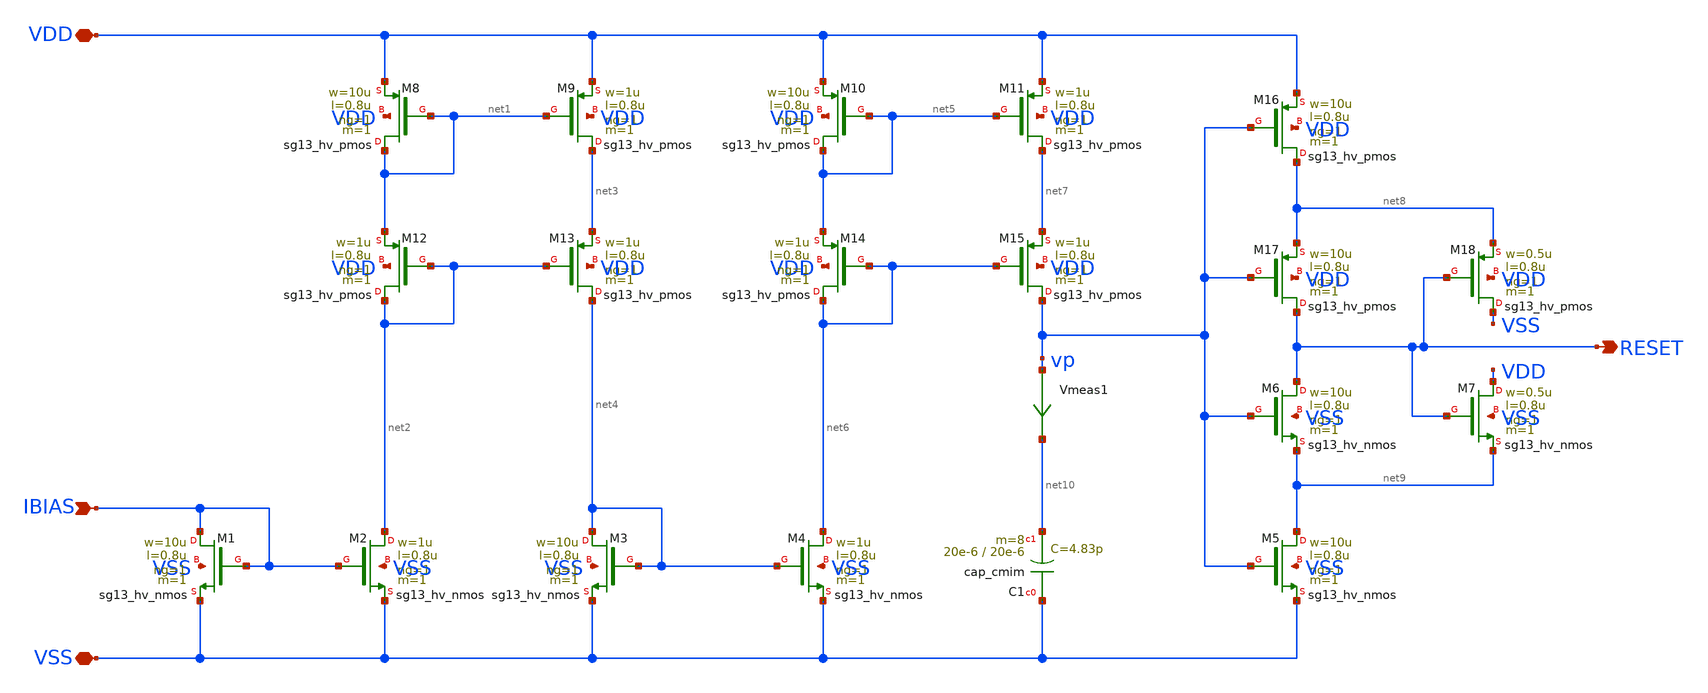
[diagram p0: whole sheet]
** sch_path: ip/por/xschem/por.sch
**.subckt por VSS VDD RESET IBIAS
*.iopin VSS
*.iopin VDD
*.opin RESET
*.ipin IBIAS
XM8 net1 net1 VDD VDD sg13_hv_pmos w=10u l=0.8u ng=1 m=1 mm_ok=1
Vmeas1 vp net10 0
.save i(vmeas1)
XM12 net2 net2 net1 VDD sg13_hv_pmos w=1u l=0.8u ng=1 m=1 mm_ok=1
XM1 IBIAS IBIAS VSS VSS sg13_hv_nmos w=10u l=0.8u ng=1 m=1 mm_ok=1
XM2 net2 IBIAS VSS VSS sg13_hv_nmos w=1u l=0.8u ng=1 m=1 mm_ok=1
XM9 net3 net1 VDD VDD sg13_hv_pmos w=1u l=0.8u ng=1 m=1 mm_ok=1
XM13 net4 net2 net3 VDD sg13_hv_pmos w=1u l=0.8u ng=1 m=1 mm_ok=1
XM3 net4 net4 VSS VSS sg13_hv_nmos w=10u l=0.8u ng=1 m=1 mm_ok=1
XM10 net5 net5 VDD VDD sg13_hv_pmos w=10u l=0.8u ng=1 m=1 mm_ok=1
XM14 net6 net6 net5 VDD sg13_hv_pmos w=1u l=0.8u ng=1 m=1 mm_ok=1
XM4 net6 net4 VSS VSS sg13_hv_nmos w=1u l=0.8u ng=1 m=1 mm_ok=1
XM11 net7 net5 VDD VDD sg13_hv_pmos w=1u l=0.8u ng=1 m=1 mm_ok=1
XM15 vp net6 net7 VDD sg13_hv_pmos w=1u l=0.8u ng=1 m=1 mm_ok=1
XC1 VSS net10 cap_cmim w=20e-6 l=20e-6 m=8 mm_ok=1
XM16 net8 vp VDD VDD sg13_hv_pmos w=10u l=0.8u ng=1 m=1 mm_ok=1
XM17 RESET vp net8 VDD sg13_hv_pmos w=10u l=0.8u ng=1 m=1 mm_ok=1
XM5 net9 vp VSS VSS sg13_hv_nmos w=10u l=0.8u ng=1 m=1 mm_ok=1
XM6 RESET vp net9 VSS sg13_hv_nmos w=10u l=0.8u ng=1 m=1 mm_ok=1
XM18 VSS RESET net8 VDD sg13_hv_pmos w=0.5u l=0.8u ng=1 m=1 mm_ok=1
XM7 VDD RESET net9 VSS sg13_hv_nmos w=0.5u l=0.8u ng=1 m=1 mm_ok=1
**.ends
.end
